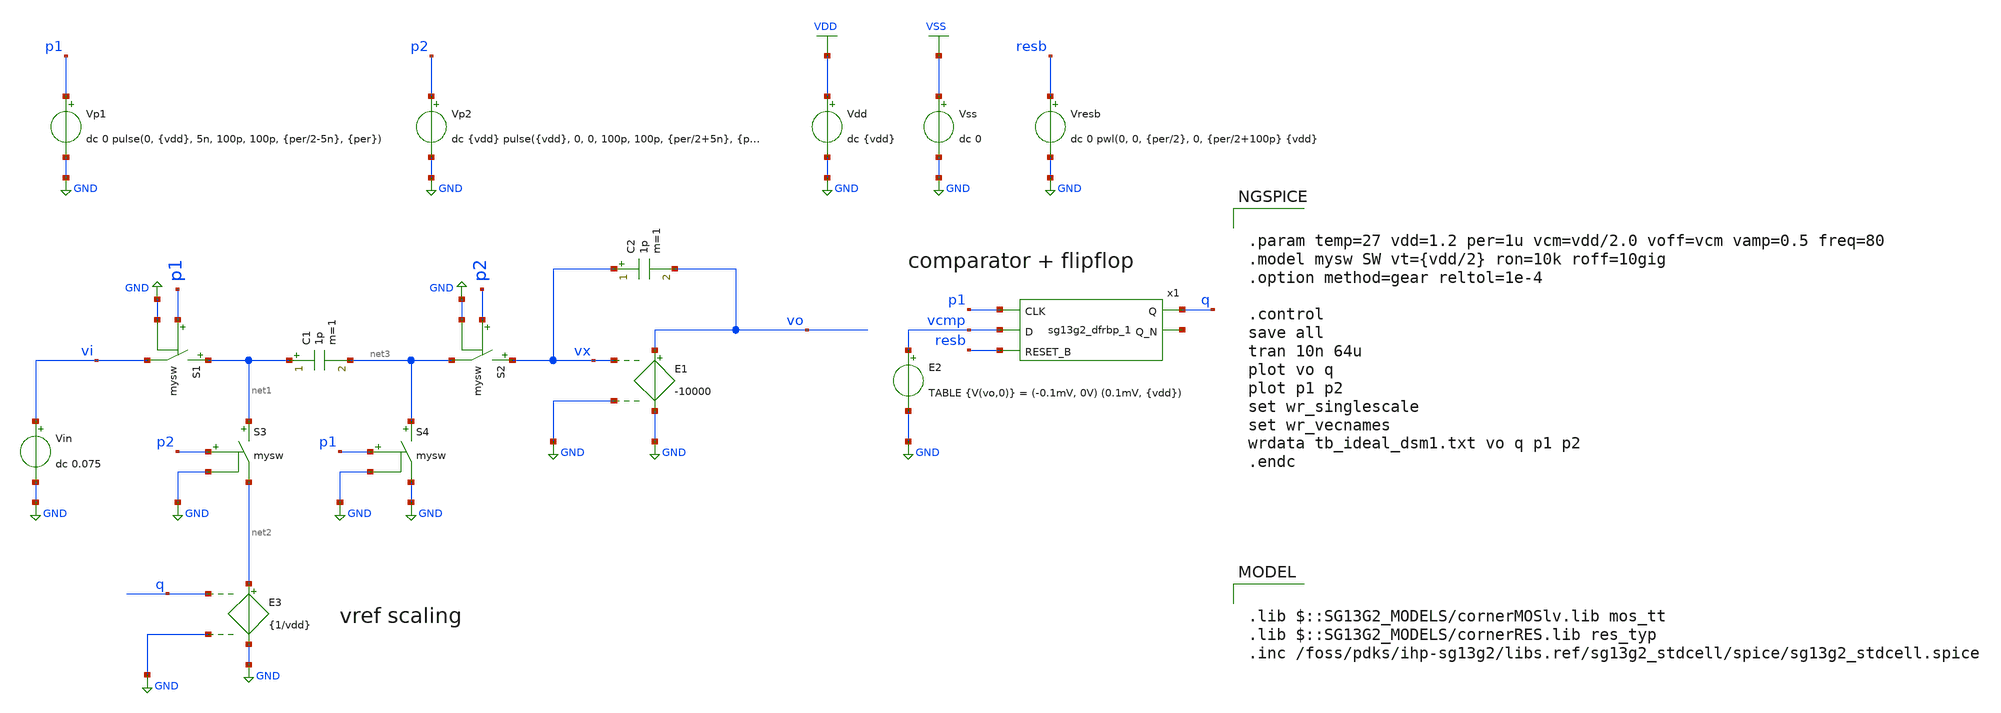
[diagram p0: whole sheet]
** sch_path: files/ic_design/2_Idealized_circuits/tb_ideal_dsm1.sch
**.subckt tb_ideal_dsm1
Vp1 p1 GND dc 0 pulse(0, {vdd}, 5n, 100p, 100p, {per/2-5n}, {per})
E1 vo GND vx GND -10000
S1 net1 vi p1 GND mysw
Vp2 p2 GND dc {vdd} pulse({vdd}, 0, 0, 100p, 100p, {per/2+5n}, {per})
Vin vi GND dc 0.075
C1 net1 net3 1p m=1
S2 vx net3 p2 GND mysw
C2 vx vo 1p m=1
S3 net1 net2 p2 GND mysw
S4 net3 GND p1 GND mysw
E2 vcmp GND TABLE {V(vo,0)} = (-0.1mV, 0V) (0.1mV, {vdd})
Vdd VDD GND dc {vdd}
E3 net2 GND q GND {1/vdd}
Vresb resb GND dc 0 pwl(0, 0, {per/2}, 0, {per/2+100p} {vdd}
x1 q net4 p1 vcmp resb VDD VSS sg13g2_dfrbp_1
Vss VSS GND dc 0
**** begin user architecture code

.lib $::SG13G2_MODELS/cornerMOSlv.lib mos_tt
.lib $::SG13G2_MODELS/cornerRES.lib res_typ
.inc /foss/pdks/ihp-sg13g2/libs.ref/sg13g2_stdcell/spice/sg13g2_stdcell.spice



.param temp=27 vdd=1.2 per=1u vcm=vdd/2.0 voff=vcm vamp=0.5 freq=80
.model mysw SW vt={vdd/2} ron=10k roff=10gig
.option method=gear reltol=1e-4

.control
save all
tran 10n 64u
plot vo q
plot p1 p2
set wr_singlescale
set wr_vecnames
wrdata tb_ideal_dsm1.txt vo q p1 p2
.endc


**** end user architecture code
**.ends

* expanding   symbol:  sg13g2_stdcells/sg13g2_dfrbp_1.sym # of pins=5
** sym_path: sg13g2_stdcells/sg13g2_dfrbp_1.sym
** sch_path: sg13g2_stdcells/sg13g2_dfrbp_1.sch
.subckt sg13g2_dfrbp_1 Q Q_N CLK D RESET_B VDD VSS
*.ipin D
*.ipin RESET_B
*.ipin CLK
*.opin Q
*.opin Q_N
*.iopin VDD
*.iopin VSS
XM1 Db D net10 VSS sg13_lv_nmos w=420.00n l=130.00n ng=1 m=1 mm_ok=1
XM2 net10 RESET_B VSS VSS sg13_lv_nmos w=420.00n l=130.00n ng=1 m=1 mm_ok=1
XM3 net1 clkneg net9 VSS sg13_lv_nmos w=420.00n l=130.00n ng=1 m=1 mm_ok=1
XM4 net9 net1 VSS VSS sg13_lv_nmos w=420.00n l=130.00n ng=1 m=1 mm_ok=1
XM5 net1 net1 net5 VSS sg13_lv_nmos w=420.00n l=130.00n ng=1 m=1 mm_ok=1
XM6 net5 RESET_B VSS VSS sg13_lv_nmos w=420.00n l=130.00n ng=1 m=1 mm_ok=1
XM7 Q_N net1 VSS VSS sg13_lv_nmos w=740.00n l=130.00n ng=1 m=1 mm_ok=1
XM8 net2 net1 VSS VSS sg13_lv_nmos w=740.00n l=130.00n ng=1 m=1 mm_ok=1
XM9 Q net2 VSS VSS sg13_lv_nmos w=740.00n l=130.00n ng=1 m=1 mm_ok=1
XM10 clkneg CLK VSS VSS sg13_lv_nmos w=740.00n l=130.00n ng=1 m=1 mm_ok=1
XM11 clkpos clkneg VSS VSS sg13_lv_nmos w=740.00n l=130.00n ng=1 m=1 mm_ok=1
XM12 Db clkneg net3 VSS sg13_lv_nmos w=420.00n l=130.00n ng=1 m=1 mm_ok=1
XM13 net3 clkpos net8 VSS sg13_lv_nmos w=420.00n l=130.00n ng=1 m=1 mm_ok=1
XM14 net8 net3 net4 VSS sg13_lv_nmos w=420.00n l=130.00n ng=1 m=1 mm_ok=1
XM15 net4 RESET_B VSS VSS sg13_lv_nmos w=420.00n l=130.00n ng=1 m=1 mm_ok=1
XM16 net3 net3 VSS VSS sg13_lv_nmos w=740.00n l=130.00n ng=1 m=1 mm_ok=1
XM17 net3 clkpos net1 VSS sg13_lv_nmos w=740.00n l=130.00n ng=1 m=1 mm_ok=1
XM18 Db RESET_B VDD VDD sg13_lv_pmos w=420.00n l=130.00n ng=1 m=1 mm_ok=1
XM19 Db D VDD VDD sg13_lv_pmos w=420.00n l=130.00n ng=1 m=1 mm_ok=1
XM20 net7 net1 VDD VDD sg13_lv_pmos w=420.00n l=130.00n ng=1 m=1 mm_ok=1
XM21 net1 clkpos net7 VDD sg13_lv_pmos w=420.00n l=130.00n ng=1 m=1 mm_ok=1
XM22 net1 net1 VDD VDD sg13_lv_pmos w=420.00n l=130.00n ng=1 m=1 mm_ok=1
XM23 net1 RESET_B VDD VDD sg13_lv_pmos w=420.00n l=130.00n ng=1 m=1 mm_ok=1
XM24 Q_N net1 VDD VDD sg13_lv_pmos w=1.12u l=130.00n ng=1 m=1 mm_ok=1
XM25 net2 net1 VDD VDD sg13_lv_pmos w=1.12u l=130.00n ng=1 m=1 mm_ok=1
XM26 Q net2 VDD VDD sg13_lv_pmos w=1.12u l=130.00n ng=1 m=1 mm_ok=1
XM27 clkneg CLK VDD VDD sg13_lv_pmos w=1.12u l=130.00n ng=1 m=1 mm_ok=1
XM28 clkpos clkneg VDD VDD sg13_lv_pmos w=1.12u l=130.00n ng=1 m=1 mm_ok=1
XM29 Db clkpos net3 VDD sg13_lv_pmos w=420.00n l=130.00n ng=1 m=1 mm_ok=1
XM30 net6 net3 VDD VDD sg13_lv_pmos w=420.00n l=130.00n ng=1 m=1 mm_ok=1
XM31 net3 clkneg net6 VDD sg13_lv_pmos w=420.00n l=130.00n ng=1 m=1 mm_ok=1
XM32 net3 RESET_B VDD VDD sg13_lv_pmos w=420.00n l=130.00n ng=1 m=1 mm_ok=1
XM33 net3 net3 VDD VDD sg13_lv_pmos w=1.000u l=130.00n ng=1 m=1 mm_ok=1
XM34 net3 clkneg net1 VDD sg13_lv_pmos w=1.000u l=130.00n ng=1 m=1 mm_ok=1
.ends

.GLOBAL GND
.GLOBAL VDD
.GLOBAL VSS
.end
